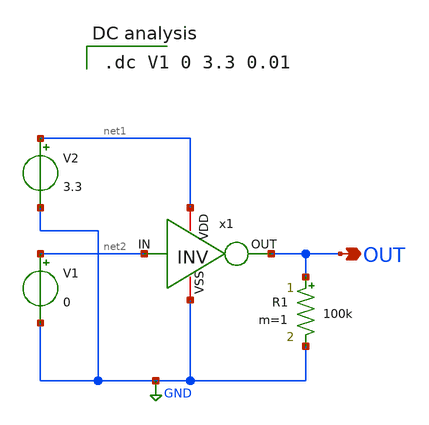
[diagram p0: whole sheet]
** sch_path: INV_sim.sch
**.subckt INV_sim OUT
*.opin OUT
x1 net1 OUT net2 GND INV
V1 net2 GND 0
V2 net1 GND 3.3
R1 OUT GND 100k m=1
**** begin user architecture code

.dc V1 0 3.3 0.01

**** end user architecture code
**.ends

* expanding   symbol:  C:/Users/ISLab2/Documents/minimal_LR/INV.sym # of pins=4
** sym_path: INV.sym
** sch_path: INV.sch
.subckt INV VDD OUT IN VSS
*.opin OUT
*.ipin IN
*.iopin VDD
*.iopin VSS
M2 OUT IN VDD VDD pch w=10u l=0.35u as=0 ps=0 ad=0 pd=0 m=1
M1 OUT IN VSS VSS nch w=5u l=0.35u as=0 ps=0 ad=0 pd=0 m=1
**** begin user architecture code


.include C:/Users/ISLab2/Documents/minimal_LR/minimal.txt

**** end user architecture code
.ends

.GLOBAL GND
.end
